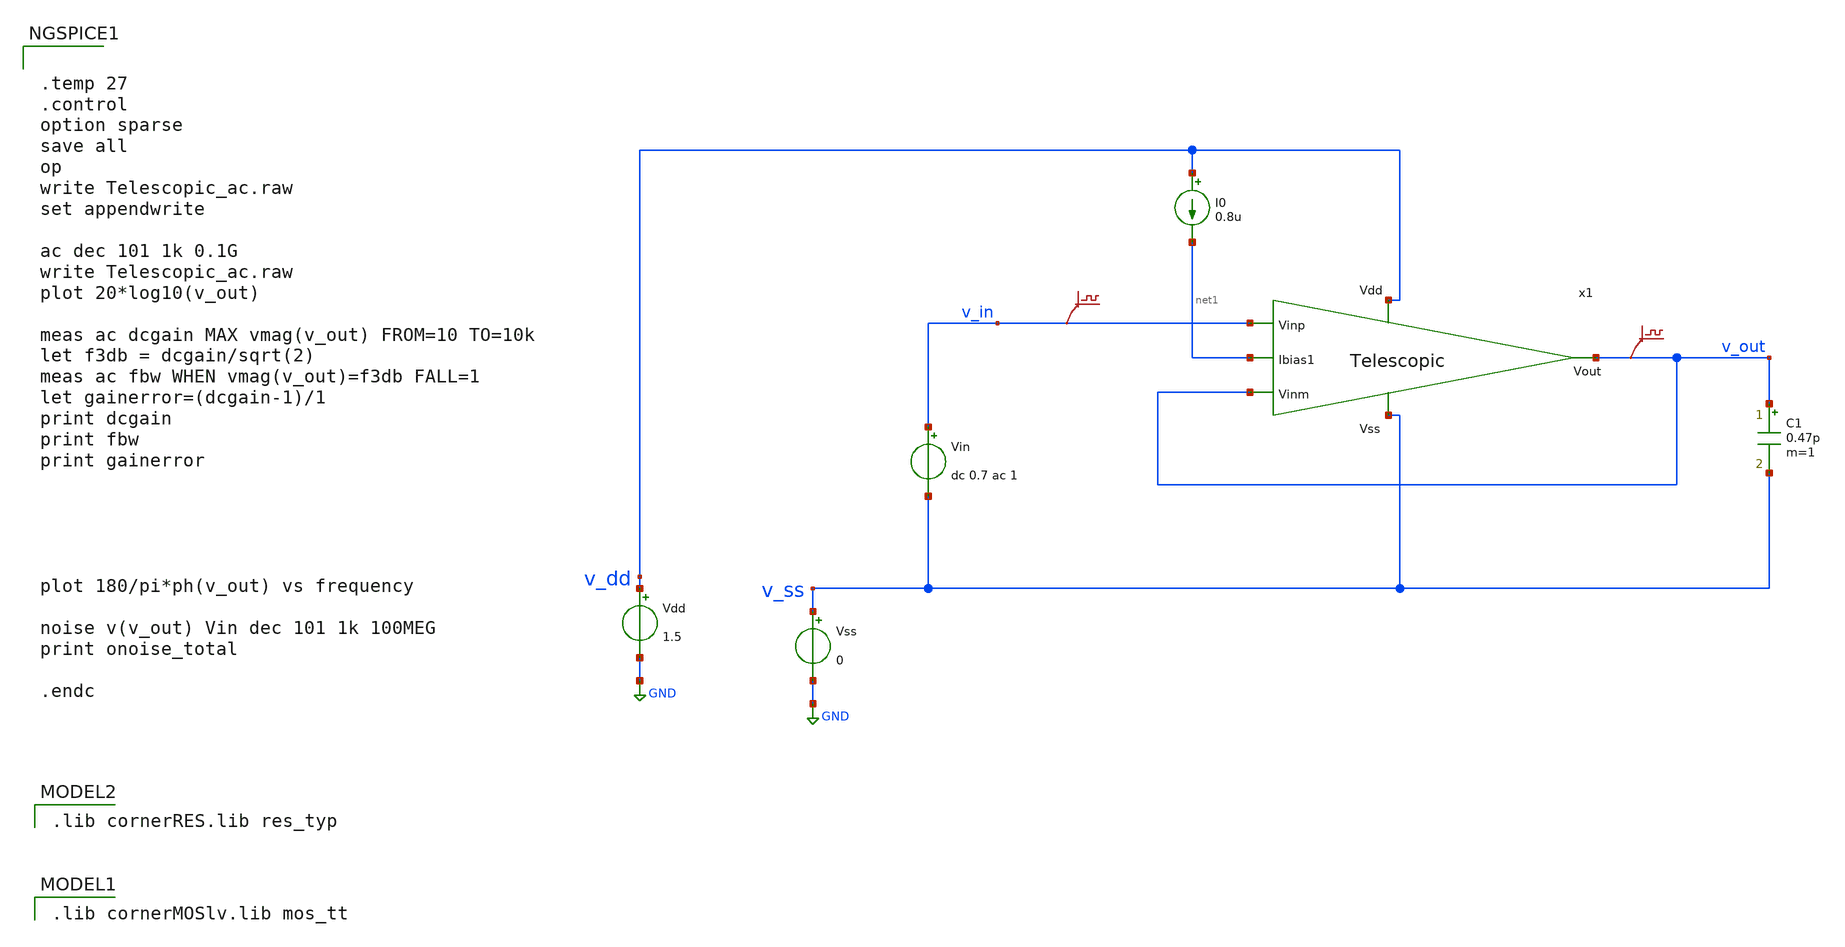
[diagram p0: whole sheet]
** sch_path: design/design_switch_cap/tb_Telescopic_ac.sch
* (c) 2024 Priyanka, @HSB
**.subckt tb_Telescopic_ac
Vss v_ss GND 0
Vdd v_dd GND 1.5
Vin v_in v_ss dc 0.7 ac 1
.save v(v_in)
I0 v_dd net1 0.8u
C1 v_out v_ss 0.47p m=1
.save v(v_out)
x1 v_dd net1 v_out v_out v_in v_ss Telescopic
**** begin user architecture code
 .lib cornerMOSlv.lib mos_tt

 .lib cornerRES.lib res_typ



.temp 27
.control
option sparse
save all
op
write Telescopic_ac.raw
set appendwrite

ac dec 101 1k 0.1G
write Telescopic_ac.raw
plot 20*log10(v_out)

meas ac dcgain MAX vmag(v_out) FROM=10 TO=10k
let f3db = dcgain/sqrt(2)
meas ac fbw WHEN vmag(v_out)=f3db FALL=1
let gainerror=(dcgain-1)/1
print dcgain
print fbw
print gainerror





plot 180/pi*ph(v_out) vs frequency

noise v(v_out) Vin dec 101 1k 100MEG
print onoise_total

.endc


**** end user architecture code
**.ends

* expanding   symbol:  Telescopic.sym # of pins=6
** sym_path: Telescopic.sym
** sch_path: Telescopic.sch
.subckt Telescopic Vdd Ibias1 Vout Vinm Vinp Vss
*.ipin Vinp
*.opin Vout
*.ipin Vinm
*.ipin Vss
*.ipin Vdd
*.ipin Ibias1
XM19 net1 net7 Vss Vss sg13_lv_nmos w=0.3u l=2u ng=1 m=1 mm_ok=1
XM11 net2 Vinp net1 Vss sg13_lv_nmos w=0.15u l=2u ng=1 m=1 mm_ok=1
XM14 net3 Vinm net1 Vss sg13_lv_nmos w=0.15u l=2u ng=1 m=1 mm_ok=1
XM20 Vout net5 net4 Vdd sg13_lv_pmos w=0.16u l=0.5u ng=1 m=1 mm_ok=1
XM25 net9 net5 net10 Vdd sg13_lv_pmos w=0.16u l=0.5u ng=1 m=1 mm_ok=1
XM1 net5 net7 Vss Vss sg13_lv_nmos w=0.15u l=2u ng=1 m=1 mm_ok=1
XM2 net8 net7 Vss Vss sg13_lv_nmos w=0.15u l=2u ng=1 m=1 mm_ok=1
XM3 Vdd Ibias1 net8 Vss sg13_lv_nmos w=0.15u l=2u ng=1 m=1 mm_ok=1
XM4 Vout Ibias1 net3 Vss sg13_lv_nmos w=0.15u l=2u ng=1 m=1 mm_ok=1
XM5 net9 Ibias1 net2 Vss sg13_lv_nmos w=0.15u l=2u ng=1 m=1 mm_ok=1
XM6 net4 net6 Vdd Vdd sg13_lv_pmos w=0.16u l=0.5u ng=1 m=1 mm_ok=1
XM7 net6 net6 Vdd Vdd sg13_lv_pmos w=0.16u l=0.5u ng=1 m=1 mm_ok=1
XM8 net5 net5 net6 Vdd sg13_lv_pmos w=0.16u l=0.5u ng=1 m=1 mm_ok=1
XM9 net10 net6 Vdd Vdd sg13_lv_pmos w=0.16u l=0.5u ng=1 m=1 mm_ok=1
XM10 net7 net7 Vss Vss sg13_lv_nmos w=0.15u l=2u ng=1 m=1 mm_ok=1
XM12 Ibias1 Ibias1 net7 Vss sg13_lv_nmos w=0.15u l=2u ng=1 m=1 mm_ok=1
.ends

.GLOBAL GND
.end
